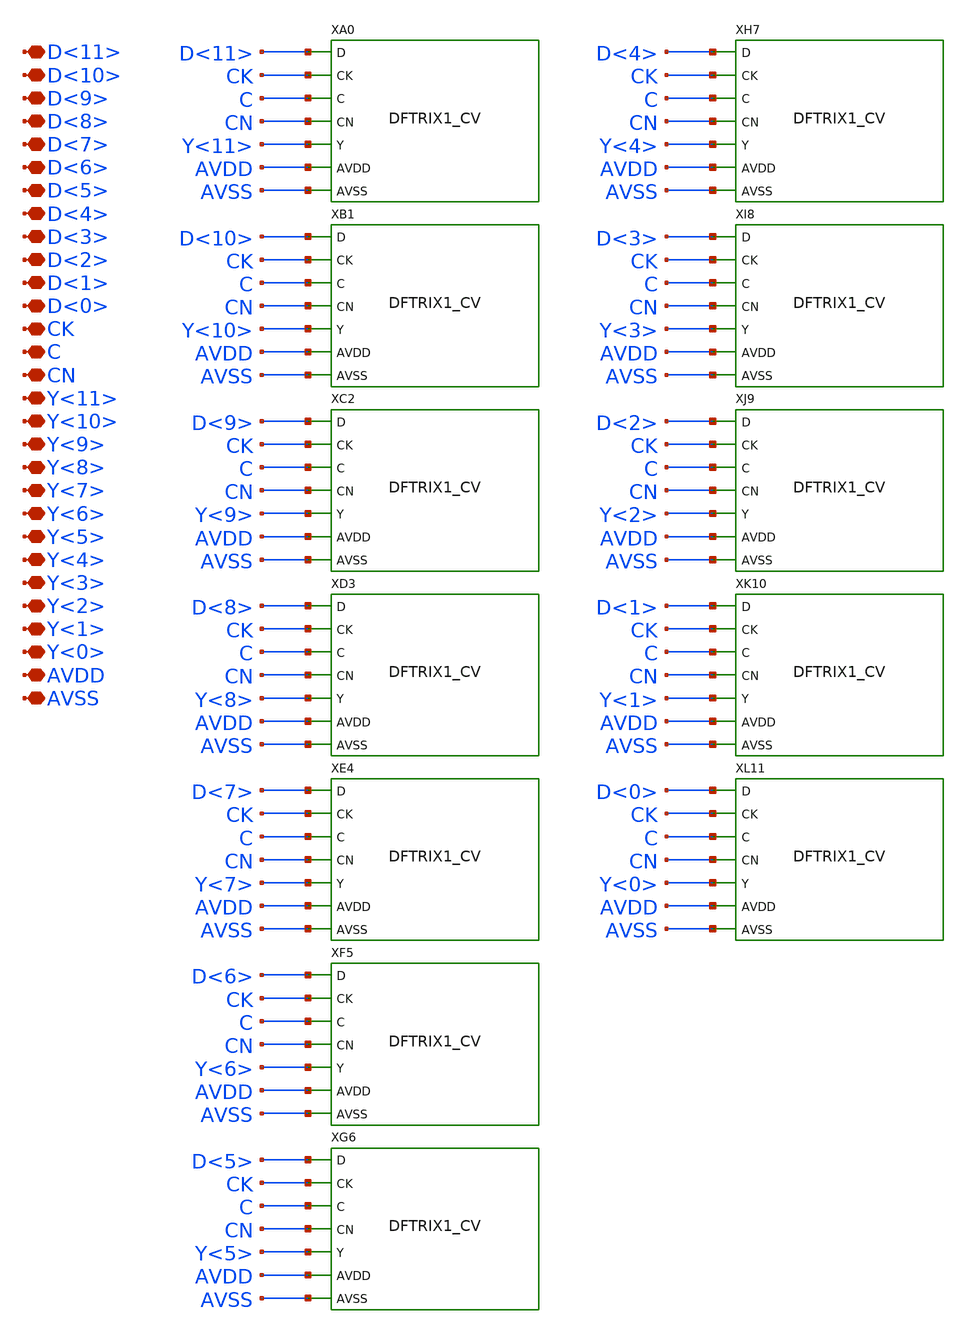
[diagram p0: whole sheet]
** sch_path: sim/SUN_TR/build/SUN_TR_SK130NM/xschem/SUN_TR_SK130NM/RG12TRIX1_CV.sch
**.subckt RG12TRIX1_CV D<11> D<10> D<9> D<8> D<7> D<6> D<5> D<4> D<3> D<2> D<1> D<0> CK C CN Y<11>
*+ Y<10> Y<9> Y<8> Y<7> Y<6> Y<5> Y<4> Y<3> Y<2> Y<1> Y<0> AVDD AVSS
*.iopin D<11>
*.iopin D<10>
*.iopin D<9>
*.iopin D<8>
*.iopin D<7>
*.iopin D<6>
*.iopin D<5>
*.iopin D<4>
*.iopin D<3>
*.iopin D<2>
*.iopin D<1>
*.iopin D<0>
*.iopin CK
*.iopin C
*.iopin CN
*.iopin Y<11>
*.iopin Y<10>
*.iopin Y<9>
*.iopin Y<8>
*.iopin Y<7>
*.iopin Y<6>
*.iopin Y<5>
*.iopin Y<4>
*.iopin Y<3>
*.iopin Y<2>
*.iopin Y<1>
*.iopin Y<0>
*.iopin AVDD
*.iopin AVSS
XA0 D<11> CK C CN Y<11> AVDD AVSS DFTRIX1_CV
XB1 D<10> CK C CN Y<10> AVDD AVSS DFTRIX1_CV
XC2 D<9> CK C CN Y<9> AVDD AVSS DFTRIX1_CV
XD3 D<8> CK C CN Y<8> AVDD AVSS DFTRIX1_CV
XE4 D<7> CK C CN Y<7> AVDD AVSS DFTRIX1_CV
XF5 D<6> CK C CN Y<6> AVDD AVSS DFTRIX1_CV
XG6 D<5> CK C CN Y<5> AVDD AVSS DFTRIX1_CV
XH7 D<4> CK C CN Y<4> AVDD AVSS DFTRIX1_CV
XI8 D<3> CK C CN Y<3> AVDD AVSS DFTRIX1_CV
XJ9 D<2> CK C CN Y<2> AVDD AVSS DFTRIX1_CV
XK10 D<1> CK C CN Y<1> AVDD AVSS DFTRIX1_CV
XL11 D<0> CK C CN Y<0> AVDD AVSS DFTRIX1_CV
**.ends
.end
